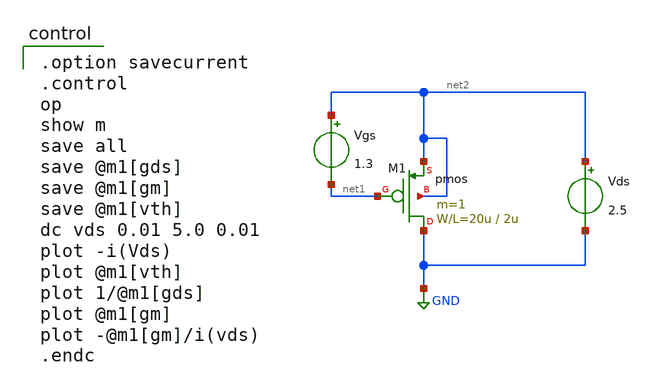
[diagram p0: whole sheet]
** sch_path: OR1/PTC06/opamp/pfet_idvds_2L.sch
**.subckt pfet_idvds_2L
Vgs net2 net1 1.3
Vds net2 GND 2.5
M1 GND net1 net2 net2 pmos L=2u W=20u m=1
**** begin user architecture code

.option savecurrent
.control
op
show m
save all
save @m1[gds]
save @m1[gm]
save @m1[vth]
dc vds 0.01 5.0 0.01
plot -i(Vds)
plot @m1[vth]
plot 1/@m1[gds]
plot @m1[gm]
plot -@m1[gm]/i(vds)
.endc

 .include $::LIB/mos.lib
.include $::LIB/passive.lib
.include $::LIB/diode.lib
**** end user architecture code
**.ends
.GLOBAL GND
.end
